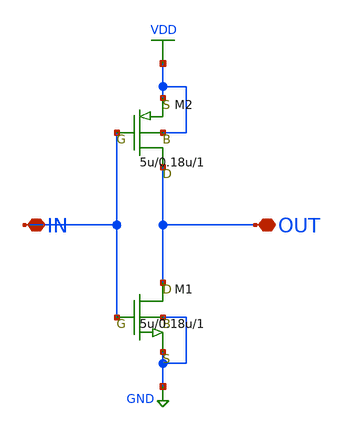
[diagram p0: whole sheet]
** sch_path: LR_hasegawa/LR_Work2/Citizen035/INVERTER_Citizen.sch
**.subckt INVERTER_Citizen OUT IN
*.iopin OUT
*.iopin IN
M1 OUT IN GND GND nch w=5u l=0.18u as=0 ps=0 ad=0 pd=0 m=1
M2 OUT IN VDD VDD pch w=5u l=0.18u as=0 ps=0 ad=0 pd=0 m=1
**.ends
.GLOBAL VDD
.GLOBAL GND
.end
